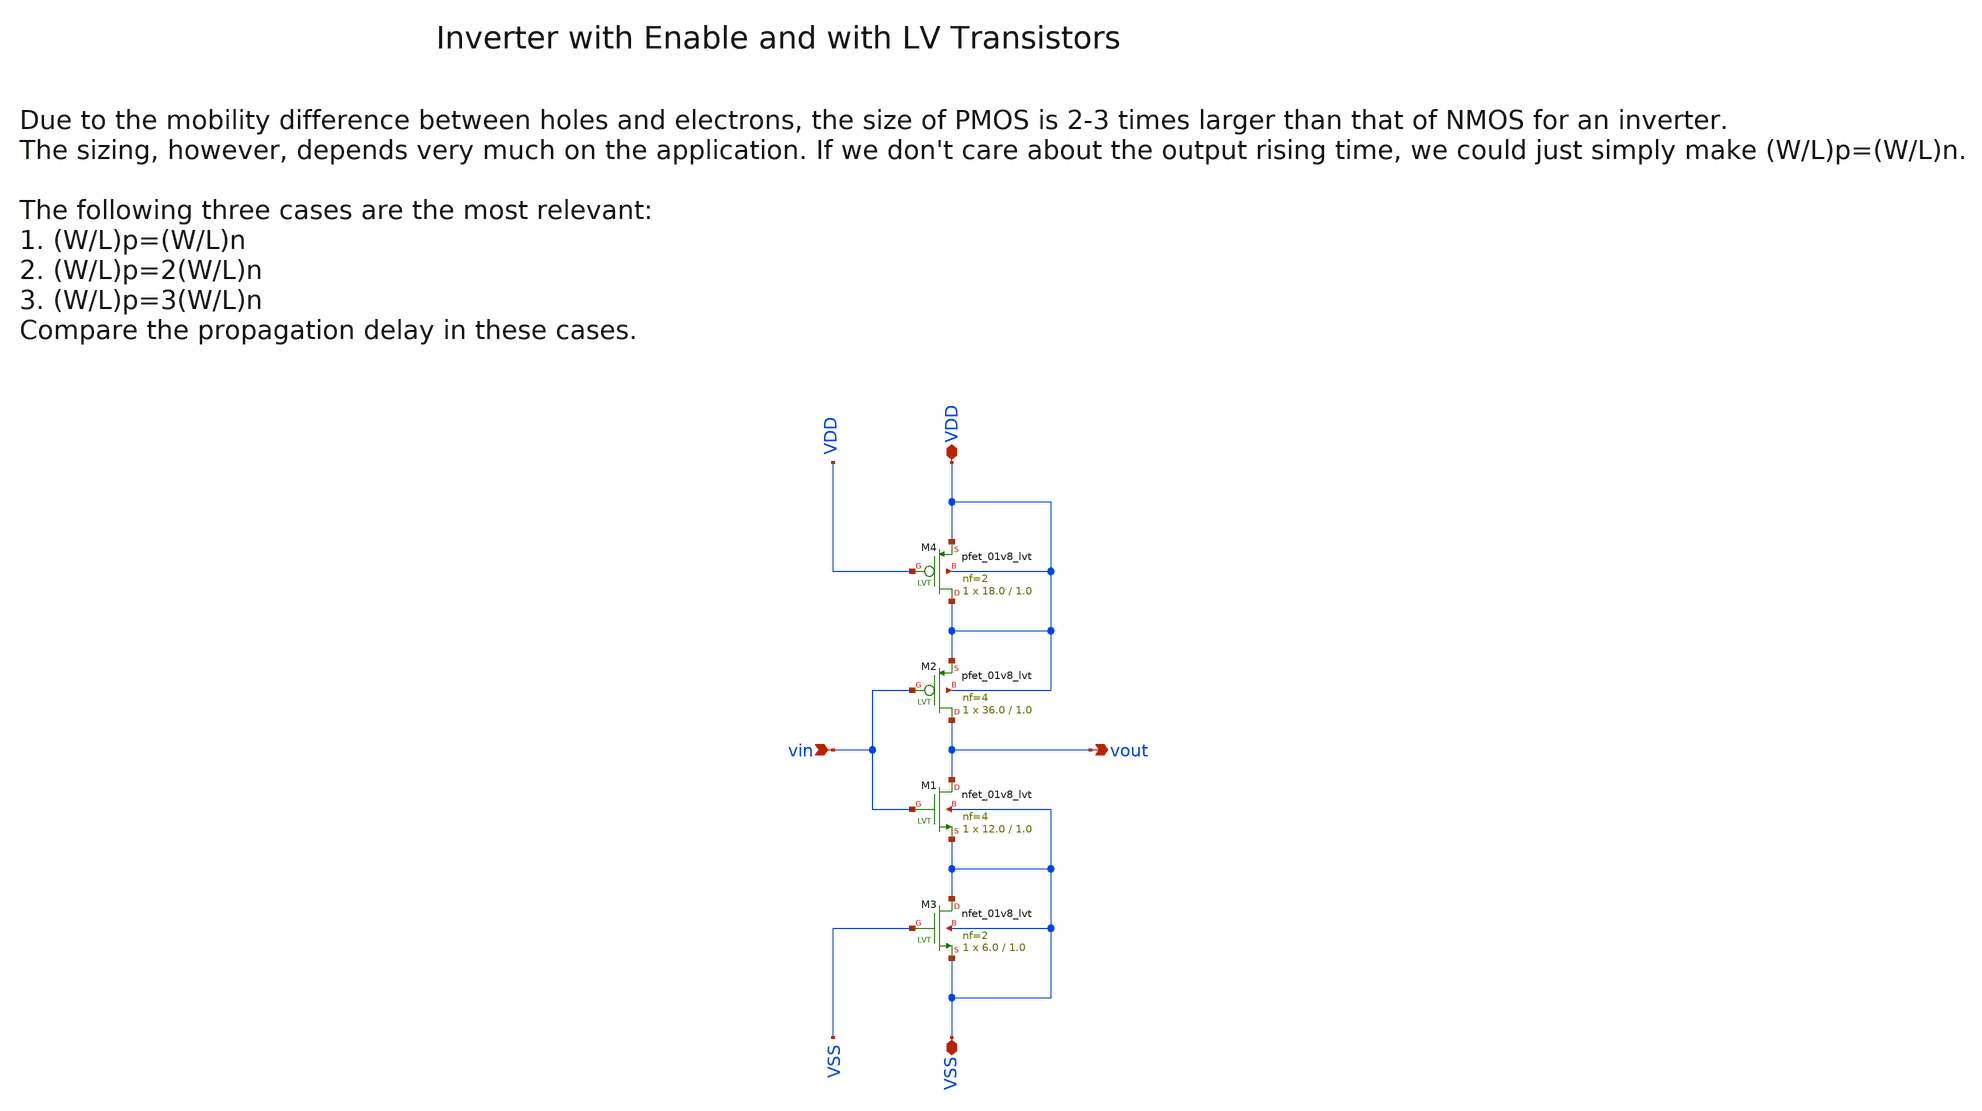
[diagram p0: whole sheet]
** sch_path: sky130/xschem/wspr_tx_iqmod_mfb_lpf_ota_core_inv_lv_NF4.sch
**.subckt wspr_tx_iqmod_mfb_lpf_ota_core_inv_lv_NF4 vin VDD VSS vout
*.ipin vin
*.iopin VDD
*.iopin VSS
*.opin vout
XM2 vout vin VDD VDD sky130_fd_pr__pfet_01v8_lvt L=1.0 W=36.0 nf=4 ad='int((4 + 1)/2) * 36.0 / 4 * 0.29'
+ as='int((4 + 2)/2) * 36.0 / 4 * 0.29' pd='2*int((4 + 1)/2) * (36.0 / 4 + 0.29)' ps='2*int((4 + 2)/2) * (36.0 / 4 + 0.29)'
+ nrd='0.29 / 36.0 ' nrs='0.29 / 36.0 ' sa=0 sb=0 sd=0 mult=1 m=1
XM3 VSS VSS VSS VSS sky130_fd_pr__nfet_01v8_lvt L=1.0 W=6.0 nf=2 ad='int((2 + 1)/2) * 6.0 / 2 * 0.29'
+ as='int((2 + 2)/2) * 6.0 / 2 * 0.29' pd='2*int((2 + 1)/2) * (6.0 / 2 + 0.29)' ps='2*int((2 + 2)/2) * (6.0 / 2 + 0.29)'
+ nrd='0.29 / 6.0 ' nrs='0.29 / 6.0 ' sa=0 sb=0 sd=0 mult=1 m=1
XM4 VDD VDD VDD VDD sky130_fd_pr__pfet_01v8_lvt L=1.0 W=18.0 nf=2 ad='int((2 + 1)/2) * 18.0 / 2 * 0.29'
+ as='int((2 + 2)/2) * 18.0 / 2 * 0.29' pd='2*int((2 + 1)/2) * (18.0 / 2 + 0.29)' ps='2*int((2 + 2)/2) * (18.0 / 2 + 0.29)'
+ nrd='0.29 / 18.0 ' nrs='0.29 / 18.0 ' sa=0 sb=0 sd=0 mult=1 m=1
XM1 vout vin VSS VSS sky130_fd_pr__nfet_01v8_lvt L=1.0 W=12.0 nf=4 ad='int((4 + 1)/2) * 12.0 / 4 * 0.29'
+ as='int((4 + 2)/2) * 12.0 / 4 * 0.29' pd='2*int((4 + 1)/2) * (12.0 / 4 + 0.29)' ps='2*int((4 + 2)/2) * (12.0 / 4 + 0.29)'
+ nrd='0.29 / 12.0 ' nrs='0.29 / 12.0 ' sa=0 sb=0 sd=0 mult=1 m=1
**.ends
.end
